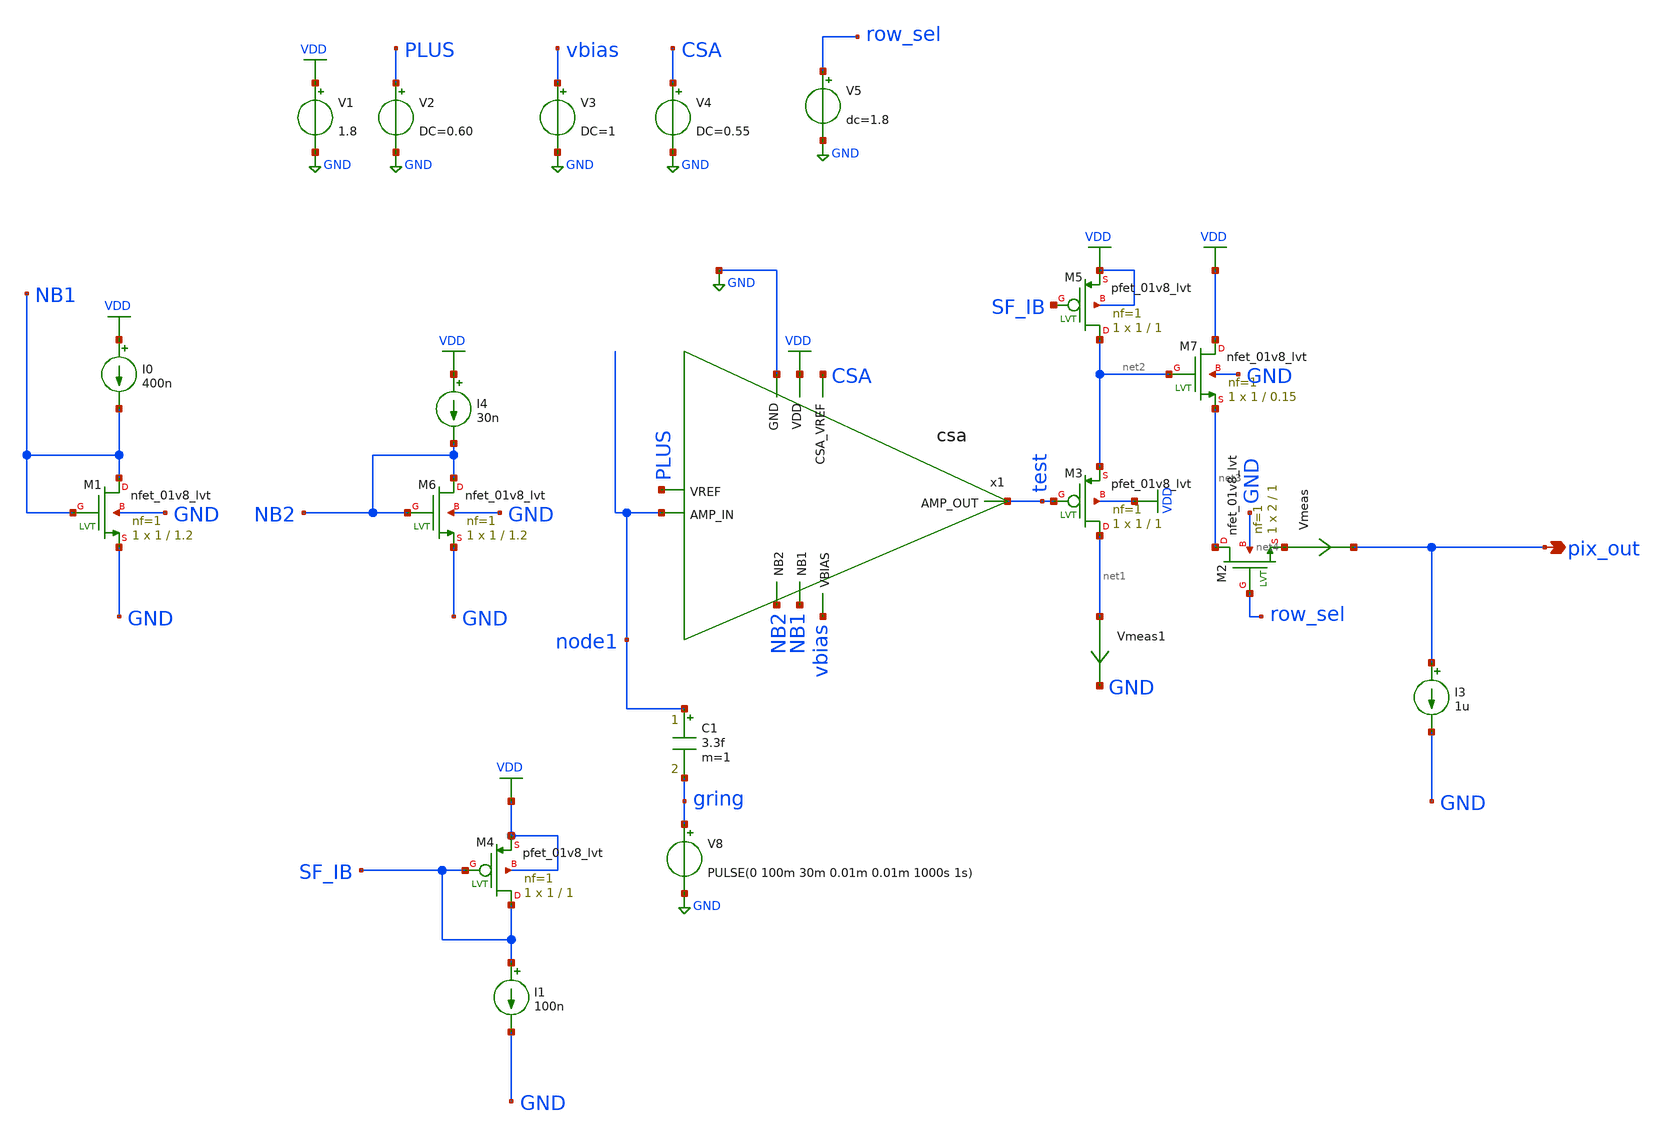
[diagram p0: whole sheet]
** sch_path: xschem/testbench/pixel_tb.sch
**.subckt pixel_tb pix_out
*.opin pix_out
V1 VDD GND 1.8
V2 PLUS GND DC=0.60
V3 vbias GND DC=1
XM1 NB1 NB1 GND GND sky130_fd_pr__nfet_01v8_lvt L=1.2 W=1 nf=1 ad='int((nf+1)/2) * W/nf * 0.29' as='int((nf+2)/2) * W/nf * 0.29'
+ pd='2*int((nf+1)/2) * (W/nf + 0.29)' ps='2*int((nf+2)/2) * (W/nf + 0.29)' nrd='0.29 / W' nrs='0.29 / W'
+ sa=0 sb=0 sd=0 mult=1 m=1
I0 VDD NB1 400n
V4 CSA GND DC=0.55
V5 row_sel GND dc=1.8
I4 VDD NB2 30n
XM6 NB2 NB2 GND GND sky130_fd_pr__nfet_01v8_lvt L=1.2 W=1 nf=1 ad='int((nf+1)/2) * W/nf * 0.29' as='int((nf+2)/2) * W/nf * 0.29'
+ pd='2*int((nf+1)/2) * (W/nf + 0.29)' ps='2*int((nf+2)/2) * (W/nf + 0.29)' nrd='0.29 / W' nrs='0.29 / W'
+ sa=0 sb=0 sd=0 mult=1 m=1
I1 SF_IB GND 100n
C1 node1 gring 3.3f m=1
V8 gring GND PULSE(0 100m 30m 0.01m 0.01m 1000s 1s)
XM4 SF_IB SF_IB VDD VDD sky130_fd_pr__pfet_01v8_lvt L=1 W=1 nf=1 ad='int((nf+1)/2) * W/nf * 0.29' as='int((nf+2)/2) * W/nf * 0.29'
+ pd='2*int((nf+1)/2) * (W/nf + 0.29)' ps='2*int((nf+2)/2) * (W/nf + 0.29)' nrd='0.29 / W' nrs='0.29 / W'
+ sa=0 sb=0 sd=0 mult=1 m=1
XM2 net3 row_sel net4 GND sky130_fd_pr__nfet_01v8_lvt L=1 W=2 nf=1 ad='int((nf+1)/2) * W/nf * 0.29' as='int((nf+2)/2) * W/nf * 0.29'
+ pd='2*int((nf+1)/2) * (W/nf + 0.29)' ps='2*int((nf+2)/2) * (W/nf + 0.29)' nrd='0.29 / W' nrs='0.29 / W'
+ sa=0 sb=0 sd=0 mult=1 m=1
XM3 net1 test net2 VDD sky130_fd_pr__pfet_01v8_lvt L=1 W=1 nf=1 ad='int((nf+1)/2) * W/nf * 0.29' as='int((nf+2)/2) * W/nf * 0.29'
+ pd='2*int((nf+1)/2) * (W/nf + 0.29)' ps='2*int((nf+2)/2) * (W/nf + 0.29)' nrd='0.29 / W' nrs='0.29 / W'
+ sa=0 sb=0 sd=0 mult=1 m=1
Vmeas net4 pix_out 0
.save i(vmeas)
XM5 net2 SF_IB VDD VDD sky130_fd_pr__pfet_01v8_lvt L=1 W=1 nf=1 ad='int((nf+1)/2) * W/nf * 0.29' as='int((nf+2)/2) * W/nf * 0.29'
+ pd='2*int((nf+1)/2) * (W/nf + 0.29)' ps='2*int((nf+2)/2) * (W/nf + 0.29)' nrd='0.29 / W' nrs='0.29 / W'
+ sa=0 sb=0 sd=0 mult=1 m=1
XM7 VDD net2 net3 GND sky130_fd_pr__nfet_01v8_lvt L=0.15 W=1 nf=1 ad='int((nf+1)/2) * W/nf * 0.29' as='int((nf+2)/2) * W/nf * 0.29'
+ pd='2*int((nf+1)/2) * (W/nf + 0.29)' ps='2*int((nf+2)/2) * (W/nf + 0.29)' nrd='0.29 / W' nrs='0.29 / W'
+ sa=0 sb=0 sd=0 mult=1 m=1
I3 pix_out GND 1u
Vmeas1 net1 GND 0
.save i(vmeas1)
x1 VDD GND test vbias PLUS node1 NB2 NB1 CSA csa
**** begin user architecture code

** opencircuitdesign pdks install
.lib $::SKYWATER_MODELS/sky130.lib.spice tt


**** end user architecture code
**.ends

* expanding   symbol:  csa.sym # of pins=9
** sym_path: xschem/csa.sym
** sch_path: xschem/csa.sch
.subckt csa VDD GND AMP_OUT VBIAS VREF AMP_IN NB2 NB1 CSA_VREF
*.ipin VREF
*.ipin AMP_IN
*.ipin NB1
*.ipin CSA_VREF
*.ipin VBIAS
*.opin AMP_OUT
*.ipin NB2
*.ipin VDD
*.ipin GND
XM2 VDD net4 AMP_OUT GND sky130_fd_pr__nfet_01v8_lvt L=1 W=1 nf=1 ad='int((nf+1)/2) * W/nf * 0.29' as='int((nf+2)/2) * W/nf * 0.29'
+ pd='2*int((nf+1)/2) * (W/nf + 0.29)' ps='2*int((nf+2)/2) * (W/nf + 0.29)' nrd='0.29 / W' nrs='0.29 / W'
+ sa=0 sb=0 sd=0 mult=1 m=1
XM8 net3 net3 net5 VDD sky130_fd_pr__pfet_01v8_lvt L=2 W=1 nf=1 ad='int((nf+1)/2) * W/nf * 0.29' as='int((nf+2)/2) * W/nf * 0.29'
+ pd='2*int((nf+1)/2) * (W/nf + 0.29)' ps='2*int((nf+2)/2) * (W/nf + 0.29)' nrd='0.29 / W' nrs='0.29 / W'
+ sa=0 sb=0 sd=0 mult=1 m=1
XM10 net6 net5 VDD VDD sky130_fd_pr__pfet_01v8_lvt L=2 W=1 nf=1 ad='int((nf+1)/2) * W/nf * 0.29' as='int((nf+2)/2) * W/nf * 0.29'
+ pd='2*int((nf+1)/2) * (W/nf + 0.29)' ps='2*int((nf+2)/2) * (W/nf + 0.29)' nrd='0.29 / W' nrs='0.29 / W'
+ sa=0 sb=0 sd=0 mult=1 m=1
XM11 net5 net5 VDD VDD sky130_fd_pr__pfet_01v8_lvt L=2 W=1 nf=1 ad='int((nf+1)/2) * W/nf * 0.29' as='int((nf+2)/2) * W/nf * 0.29'
+ pd='2*int((nf+1)/2) * (W/nf + 0.29)' ps='2*int((nf+2)/2) * (W/nf + 0.29)' nrd='0.29 / W' nrs='0.29 / W'
+ sa=0 sb=0 sd=0 mult=1 m=1
XM15 AMP_OUT NB2 GND GND sky130_fd_pr__nfet_01v8_lvt L=1.2 W=1 nf=1 ad='int((nf+1)/2) * W/nf * 0.29'
+ as='int((nf+2)/2) * W/nf * 0.29' pd='2*int((nf+1)/2) * (W/nf + 0.29)' ps='2*int((nf+2)/2) * (W/nf + 0.29)'
+ nrd='0.29 / W' nrs='0.29 / W' sa=0 sb=0 sd=0 mult=1 m=1
XM16 net2 NB1 GND GND sky130_fd_pr__nfet_01v8_lvt L=1 W=1.2 nf=1 ad='int((nf+1)/2) * W/nf * 0.29' as='int((nf+2)/2) * W/nf * 0.29'
+ pd='2*int((nf+1)/2) * (W/nf + 0.29)' ps='2*int((nf+2)/2) * (W/nf + 0.29)' nrd='0.29 / W' nrs='0.29 / W'
+ sa=0 sb=0 sd=0 mult=1 m=1
XC3 AMP_IN AMP_OUT sky130_fd_pr__cap_mim_m3_1 W=2 L=2 MF=1 m=1
XM4 net1 VREF net2 GND sky130_fd_pr__nfet_01v8_lvt L=0.15 W=7 nf=1 ad='int((nf+1)/2) * W/nf * 0.29' as='int((nf+2)/2) * W/nf * 0.29'
+ pd='2*int((nf+1)/2) * (W/nf + 0.29)' ps='2*int((nf+2)/2) * (W/nf + 0.29)' nrd='0.29 / W' nrs='0.29 / W'
+ sa=0 sb=0 sd=0 mult=1 m=1
XM7 AMP_IN CSA_VREF AMP_OUT VDD sky130_fd_pr__pfet_01v8_lvt L=8 W=0.42 nf=1 ad='int((nf+1)/2) * W/nf * 0.29'
+ as='int((nf+2)/2) * W/nf * 0.29' pd='2*int((nf+1)/2) * (W/nf + 0.29)' ps='2*int((nf+2)/2) * (W/nf + 0.29)'
+ nrd='0.29 / W' nrs='0.29 / W' sa=0 sb=0 sd=0 mult=1 m=1
XM5 net4 net3 net6 VDD sky130_fd_pr__pfet_01v8_lvt L=2 W=1 nf=1 ad='int((nf+1)/2) * W/nf * 0.29' as='int((nf+2)/2) * W/nf * 0.29'
+ pd='2*int((nf+1)/2) * (W/nf + 0.29)' ps='2*int((nf+2)/2) * (W/nf + 0.29)' nrd='0.29 / W' nrs='0.29 / W'
+ sa=0 sb=0 sd=0 mult=1 m=1
XM1 net3 VBIAS net1 GND sky130_fd_pr__nfet_01v8_lvt L=0.8 W=1 nf=1 ad='int((nf+1)/2) * W/nf * 0.29' as='int((nf+2)/2) * W/nf * 0.29'
+ pd='2*int((nf+1)/2) * (W/nf + 0.29)' ps='2*int((nf+2)/2) * (W/nf + 0.29)' nrd='0.29 / W' nrs='0.29 / W'
+ sa=0 sb=0 sd=0 mult=1 m=1
XM3 net7 AMP_IN net2 GND sky130_fd_pr__nfet_01v8_lvt L=0.15 W=7 nf=1 ad='int((nf+1)/2) * W/nf * 0.29'
+ as='int((nf+2)/2) * W/nf * 0.29' pd='2*int((nf+1)/2) * (W/nf + 0.29)' ps='2*int((nf+2)/2) * (W/nf + 0.29)'
+ nrd='0.29 / W' nrs='0.29 / W' sa=0 sb=0 sd=0 mult=1 m=1
XM6 net4 VBIAS net7 GND sky130_fd_pr__nfet_01v8_lvt L=0.8 W=1 nf=1 ad='int((nf+1)/2) * W/nf * 0.29' as='int((nf+2)/2) * W/nf * 0.29'
+ pd='2*int((nf+1)/2) * (W/nf + 0.29)' ps='2*int((nf+2)/2) * (W/nf + 0.29)' nrd='0.29 / W' nrs='0.29 / W'
+ sa=0 sb=0 sd=0 mult=1 m=1
.ends

.GLOBAL VDD
.GLOBAL GND
**** begin user architecture code


.options gmin=0.0000000000000000000001
*.options savecurrents

.control
save all
set filetype=ascii
tran 1m 100m
*plot v(test)
plot v(pix_out)

*noise v(PIX_OUT) V8 dec 10 1 1Meg
*setplot noise2
*print onoise_total

*noise v(PIX_OUT) V8 dec 10 1 1Meg
*setplot noise2
*print onoise_total
wrdata csa_output_55.txt v(pix_out) v(gring)
.endc


**** end user architecture code
.end
